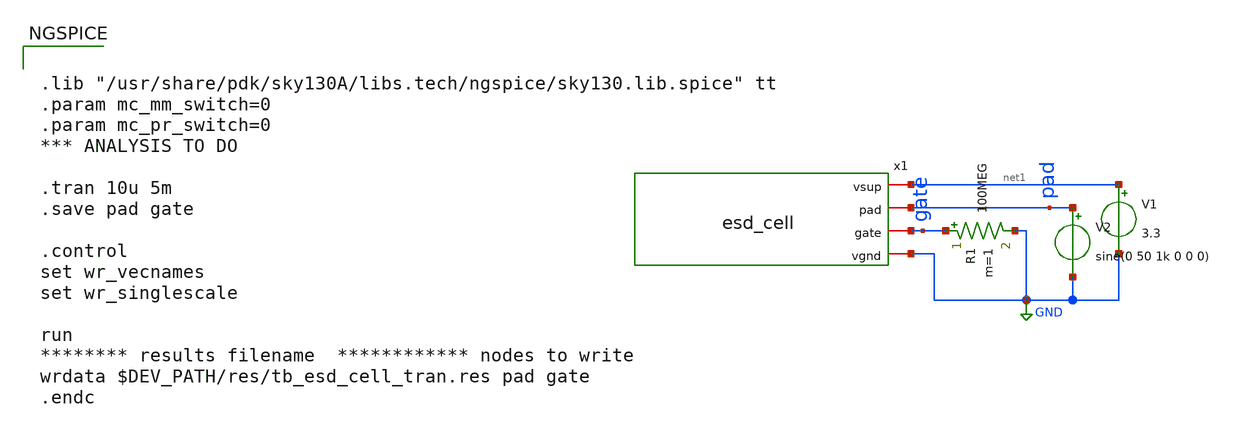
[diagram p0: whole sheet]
** sch_path: dev/esd_cell/tb/tb_esd_cell_tran.sch
**.subckt tb_esd_cell_tran
x1 net1 pad gate GND esd_cell
V1 net1 GND 3.3
V2 pad GND sine(0 50 1k 0 0 0)
R1 gate GND 100MEG m=1
**** begin user architecture code


.lib "/usr/share/pdk/sky130A/libs.tech/ngspice/sky130.lib.spice" tt
.param mc_mm_switch=0
.param mc_pr_switch=0
*** ANALYSIS TO DO

.tran 10u 5m
.save pad gate

.control
set wr_vecnames
set wr_singlescale

run
******** results filename  ************ nodes to write
wrdata $DEV_PATH/res/tb_esd_cell_tran.res pad gate
.endc


**** end user architecture code
**.ends

* expanding   symbol:  esd_cell.sym # of pins=4
** sym_path: dev/esd_cell/tb/esd_cell.sym
** sch_path: dev/esd_cell/tb/esd_cell.sch
.subckt esd_cell vsup pad gate vgnd
*.iopin vsup
*.iopin pad
*.iopin vgnd
*.iopin gate
XD1 pad vsup sky130_fd_pr__diode_pd2nw_11v0 area=10e+18 pj=4e6
XD3 gate vsup sky130_fd_pr__diode_pd2nw_05v5 area=0.203e+18 pj=4e6
XD4 vgnd gate sky130_fd_pr__diode_pw2nd_05v5 area=0.203e+18 pj=4e6
XR1 gate pad vgnd sky130_fd_pr__res_high_po W=0.35 L=10 mult=1 m=1
XD8 vgnd pad sky130_fd_pr__diode_pw2nd_11v0 area=10e+18 pj=4e6
XD2 pad vsup sky130_fd_pr__diode_pd2nw_11v0 area=10e+18 pj=4e6
XD5 pad vsup sky130_fd_pr__diode_pd2nw_11v0 area=10e+18 pj=4e6
XD6 pad vsup sky130_fd_pr__diode_pd2nw_11v0 area=10e+18 pj=4e6
XD7 pad vsup sky130_fd_pr__diode_pd2nw_11v0 area=10e+18 pj=4e6
XD9 vgnd pad sky130_fd_pr__diode_pw2nd_11v0 area=10e+18 pj=4e6
XD10 vgnd pad sky130_fd_pr__diode_pw2nd_11v0 area=10e+18 pj=4e6
XD11 vgnd pad sky130_fd_pr__diode_pw2nd_11v0 area=10e+18 pj=4e6
XD12 vgnd pad sky130_fd_pr__diode_pw2nd_11v0 area=10e+18 pj=4e6
.ends

.GLOBAL GND
.end
